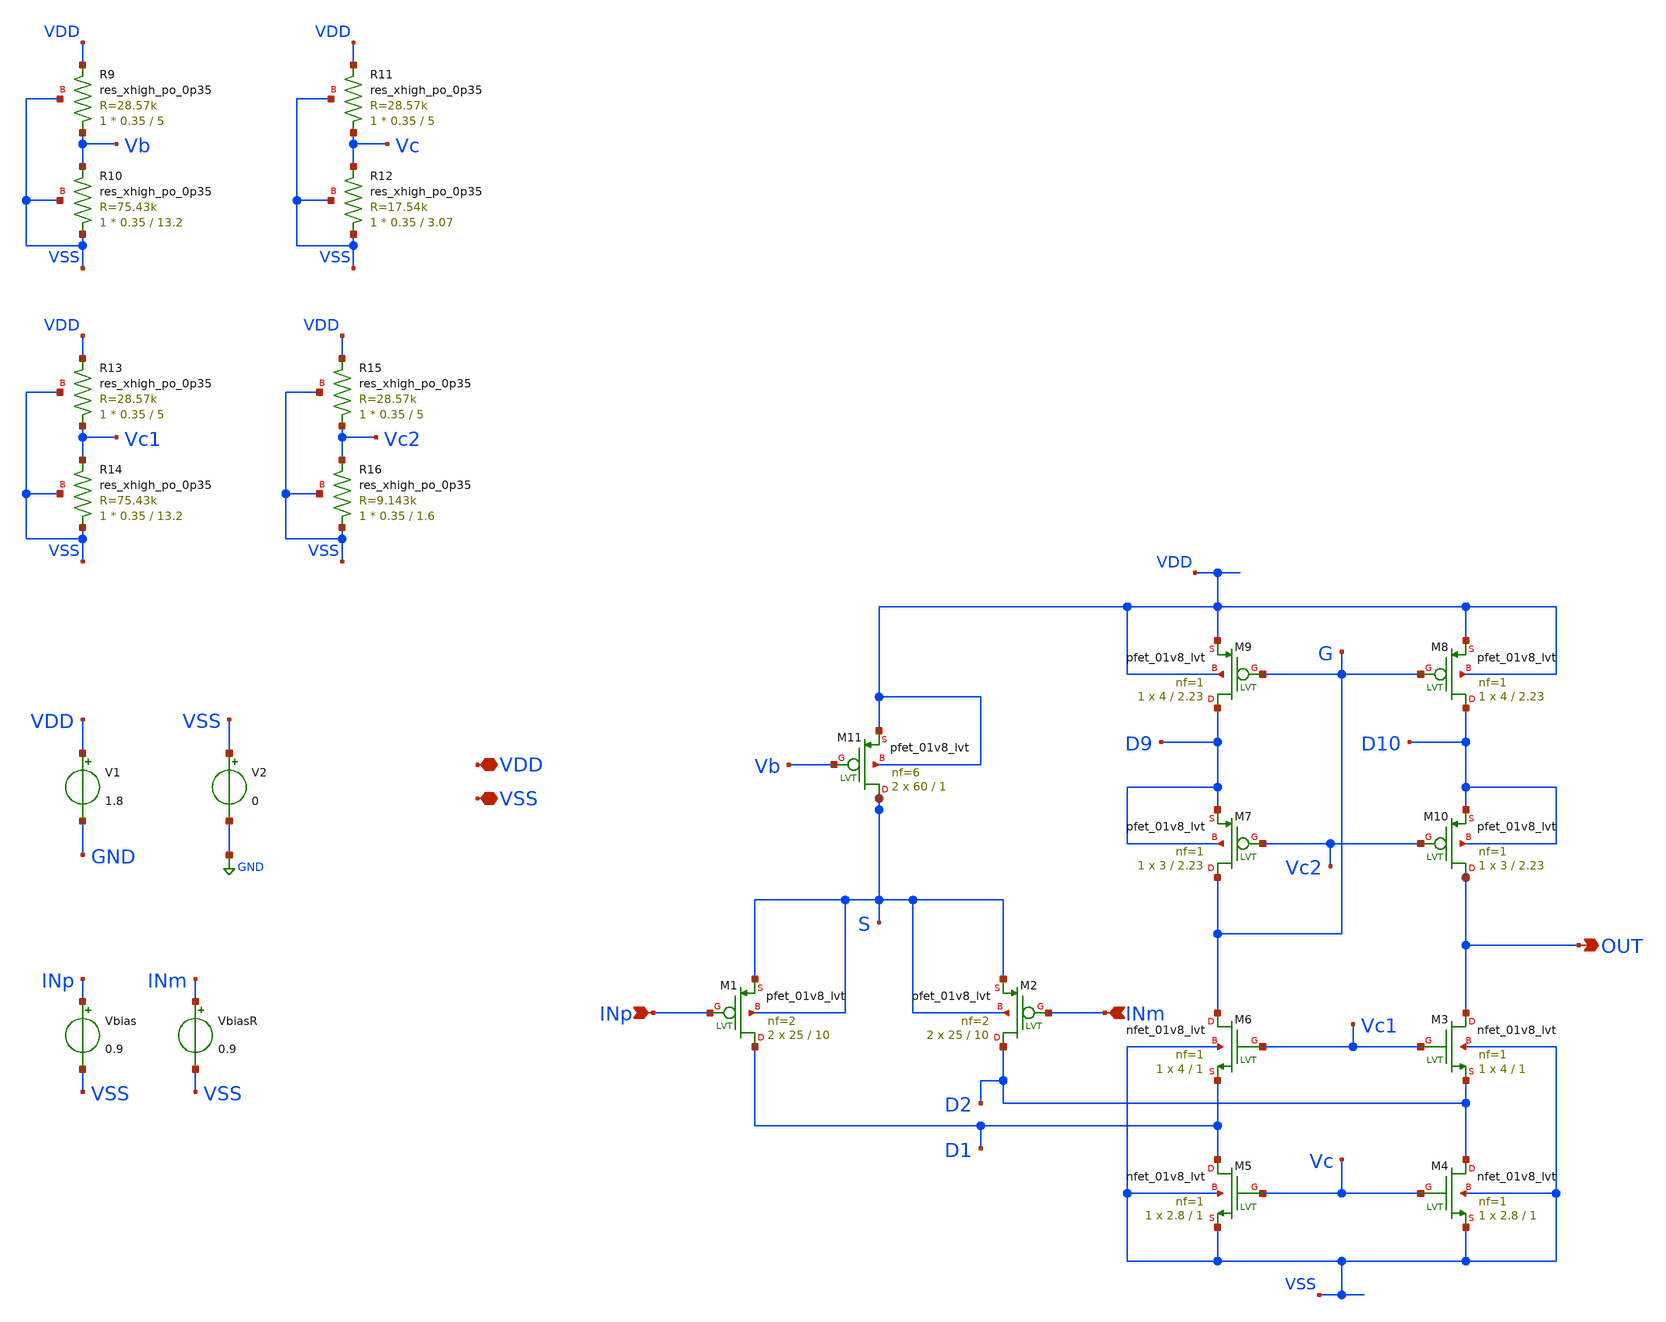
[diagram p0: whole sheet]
** sch_path: xschem/OFC_sim.sch
**.subckt OFC_sim VDD VSS INp INm OUT
*.iopin VDD
*.iopin VSS
*.ipin INp
*.ipin INm
*.opin OUT
V1 VDD GND 1.8
Vbias INp VSS 0.9
VbiasR INm VSS 0.9
V2 VSS GND 0
XR9 Vb VDD VSS sky130_fd_pr__res_xhigh_po_0p35 L=5 mult=1 m=1
XR10 VSS Vb VSS sky130_fd_pr__res_xhigh_po_0p35 L=13.2 mult=1 m=1
XR11 Vc VDD VSS sky130_fd_pr__res_xhigh_po_0p35 L=5 mult=1 m=1
XR12 VSS Vc VSS sky130_fd_pr__res_xhigh_po_0p35 L=3.07 mult=1 m=1
XR13 Vc1 VDD VSS sky130_fd_pr__res_xhigh_po_0p35 L=5 mult=1 m=1
XR14 VSS Vc1 VSS sky130_fd_pr__res_xhigh_po_0p35 L=13.2 mult=1 m=1
XR15 Vc2 VDD VSS sky130_fd_pr__res_xhigh_po_0p35 L=5 mult=1 m=1
XR16 VSS Vc2 VSS sky130_fd_pr__res_xhigh_po_0p35 L=1.6 mult=1 m=1
XM11 S Vb VDD VDD sky130_fd_pr__pfet_01v8_lvt L=1 W=60 nf=6 ad='int((nf+1)/2) * W/nf * 0.29' as='int((nf+2)/2) * W/nf * 0.29'
+ pd='2*int((nf+1)/2) * (W/nf + 0.29)' ps='2*int((nf+2)/2) * (W/nf + 0.29)' nrd='0.29 / W' nrs='0.29 / W'
+ sa=0 sb=0 sd=0 mult=2 m=2
XM1 D1 INp S S sky130_fd_pr__pfet_01v8_lvt L=10 W=25 nf=2 ad='int((nf+1)/2) * W/nf * 0.29' as='int((nf+2)/2) * W/nf * 0.29'
+ pd='2*int((nf+1)/2) * (W/nf + 0.29)' ps='2*int((nf+2)/2) * (W/nf + 0.29)' nrd='0.29 / W' nrs='0.29 / W'
+ sa=0 sb=0 sd=0 mult=2 m=2
XM2 D2 INm S S sky130_fd_pr__pfet_01v8_lvt L=10 W=25 nf=2 ad='int((nf+1)/2) * W/nf * 0.29' as='int((nf+2)/2) * W/nf * 0.29'
+ pd='2*int((nf+1)/2) * (W/nf + 0.29)' ps='2*int((nf+2)/2) * (W/nf + 0.29)' nrd='0.29 / W' nrs='0.29 / W'
+ sa=0 sb=0 sd=0 mult=2 m=2
XM3 OUT Vc1 D2 VSS sky130_fd_pr__nfet_01v8_lvt L=1 W=4 nf=1 ad='int((nf+1)/2) * W/nf * 0.29' as='int((nf+2)/2) * W/nf * 0.29'
+ pd='2*int((nf+1)/2) * (W/nf + 0.29)' ps='2*int((nf+2)/2) * (W/nf + 0.29)' nrd='0.29 / W' nrs='0.29 / W'
+ sa=0 sb=0 sd=0 mult=1 m=1
XM4 D2 Vc VSS VSS sky130_fd_pr__nfet_01v8_lvt L=1 W=2.8 nf=1 ad='int((nf+1)/2) * W/nf * 0.29' as='int((nf+2)/2) * W/nf * 0.29'
+ pd='2*int((nf+1)/2) * (W/nf + 0.29)' ps='2*int((nf+2)/2) * (W/nf + 0.29)' nrd='0.29 / W' nrs='0.29 / W'
+ sa=0 sb=0 sd=0 mult=1 m=1
XM5 D1 Vc VSS VSS sky130_fd_pr__nfet_01v8_lvt L=1 W=2.8 nf=1 ad='int((nf+1)/2) * W/nf * 0.29' as='int((nf+2)/2) * W/nf * 0.29'
+ pd='2*int((nf+1)/2) * (W/nf + 0.29)' ps='2*int((nf+2)/2) * (W/nf + 0.29)' nrd='0.29 / W' nrs='0.29 / W'
+ sa=0 sb=0 sd=0 mult=1 m=1
XM6 G Vc1 D1 VSS sky130_fd_pr__nfet_01v8_lvt L=1 W=4 nf=1 ad='int((nf+1)/2) * W/nf * 0.29' as='int((nf+2)/2) * W/nf * 0.29'
+ pd='2*int((nf+1)/2) * (W/nf + 0.29)' ps='2*int((nf+2)/2) * (W/nf + 0.29)' nrd='0.29 / W' nrs='0.29 / W'
+ sa=0 sb=0 sd=0 mult=1 m=1
XM7 G Vc2 D9 D9 sky130_fd_pr__pfet_01v8_lvt L=2.23 W=3 nf=1 ad='int((nf+1)/2) * W/nf * 0.29' as='int((nf+2)/2) * W/nf * 0.29'
+ pd='2*int((nf+1)/2) * (W/nf + 0.29)' ps='2*int((nf+2)/2) * (W/nf + 0.29)' nrd='0.29 / W' nrs='0.29 / W'
+ sa=0 sb=0 sd=0 mult=1 m=1
XM9 D9 G VDD VDD sky130_fd_pr__pfet_01v8_lvt L=2.23 W=4 nf=1 ad='int((nf+1)/2) * W/nf * 0.29' as='int((nf+2)/2) * W/nf * 0.29'
+ pd='2*int((nf+1)/2) * (W/nf + 0.29)' ps='2*int((nf+2)/2) * (W/nf + 0.29)' nrd='0.29 / W' nrs='0.29 / W'
+ sa=0 sb=0 sd=0 mult=1 m=1
XM8 D10 G VDD VDD sky130_fd_pr__pfet_01v8_lvt L=2.23 W=4 nf=1 ad='int((nf+1)/2) * W/nf * 0.29' as='int((nf+2)/2) * W/nf * 0.29'
+ pd='2*int((nf+1)/2) * (W/nf + 0.29)' ps='2*int((nf+2)/2) * (W/nf + 0.29)' nrd='0.29 / W' nrs='0.29 / W'
+ sa=0 sb=0 sd=0 mult=1 m=1
XM10 OUT Vc2 D10 D10 sky130_fd_pr__pfet_01v8_lvt L=2.23 W=3 nf=1 ad='int((nf+1)/2) * W/nf * 0.29' as='int((nf+2)/2) * W/nf * 0.29'
+ pd='2*int((nf+1)/2) * (W/nf + 0.29)' ps='2*int((nf+2)/2) * (W/nf + 0.29)' nrd='0.29 / W' nrs='0.29 / W'
+ sa=0 sb=0 sd=0 mult=1 m=1
**** begin user architecture code



* ngspice commands

.options savecurrents

.control
save all
save @m.xm1.msky130_fd_pr__pfet_01v8_lvt[gm]
save @m.xm2.msky130_fd_pr__pfet_01v8_lvt[gm]
save @m.xm3.msky130_fd_pr__nfet_01v8_lvt[gm]
save @m.xm4.msky130_fd_pr__nfet_01v8_lvt[gm]
save @m.xm5.msky130_fd_pr__nfet_01v8_lvt[gm]
save @m.xm6.msky130_fd_pr__nfet_01v8_lvt[gm]
save @m.xm7.msky130_fd_pr__pfet_01v8_lvt[gm]
save @m.xm8.msky130_fd_pr__pfet_01v8_lvt[gm]
save @m.xm9.msky130_fd_pr__pfet_01v8_lvt[gm]
save @m.xm10.msky130_fd_pr__pfet_01v8_lvt[gm]

   op
   remzerovec
   write OFC_sim.raw
   set appendwrite
   *dc Vbias 0.899 0.901 0.00001
   *dc Vbias 0.899 0.901 0.0001
   dc Vbias 0 1.8 0.01
   *remzerovec
   plot v(out),v(inp)
   plot deriv(v(out))

   write OFC_sim.raw

.endc
.end



.lib $::SKYWATER_MODELS/sky130.lib.spice tt
**** end user architecture code
**.ends
.GLOBAL GND
.end
